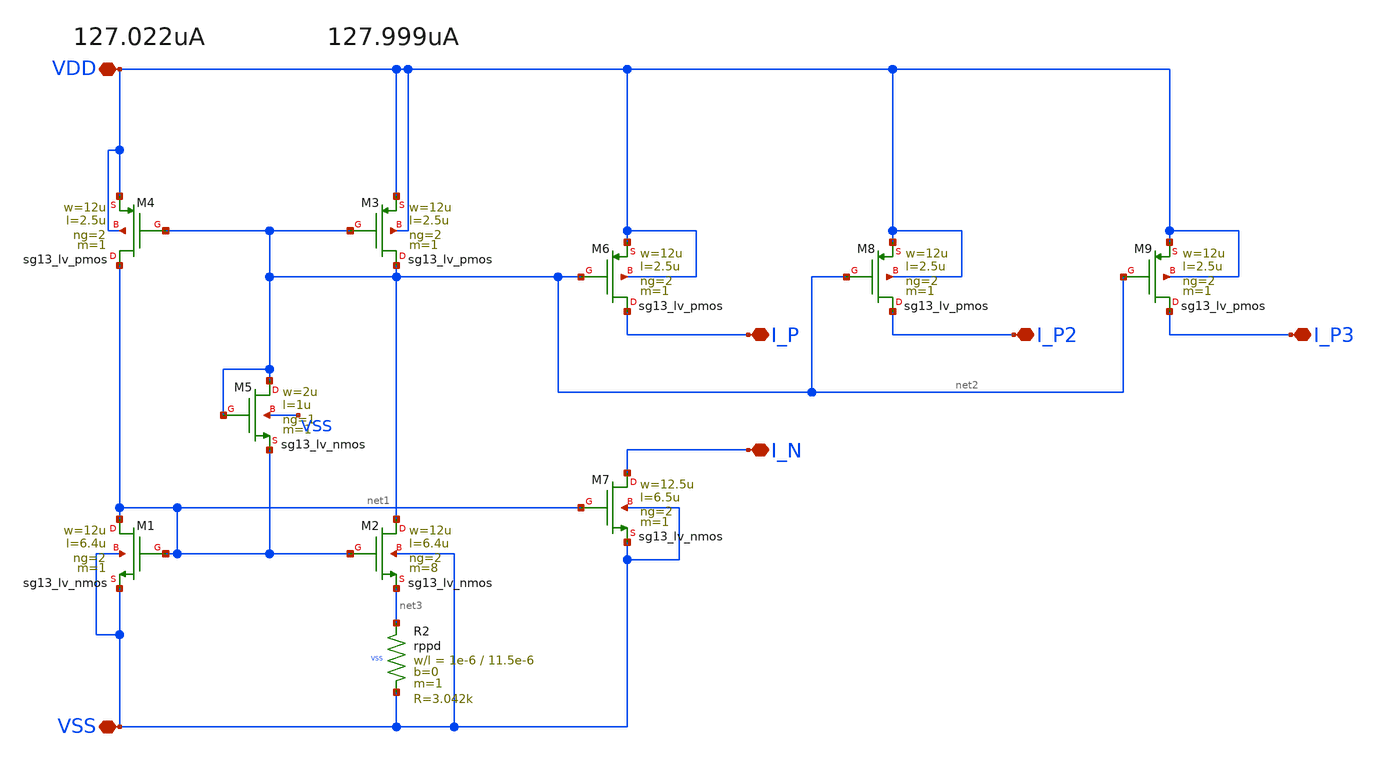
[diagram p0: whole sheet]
** sch_path: OTA_Telescopic_NO_FLATTEN/Schematics_and_Symbols/OTA_Telescopic_currentRef.sch
**.subckt OTA_Telescopic_currentRef VDD VSS I_P I_N I_P2 I_P3
*.iopin VDD
*.iopin VSS
*.iopin I_P
*.iopin I_N
*.iopin I_P2
*.iopin I_P3
XM3 net2 net2 VDD VDD sg13_lv_pmos w=12u l=2.5u ng=2 m=1 mm_ok=1
XM2 net2 net1 net3 VSS sg13_lv_nmos w=12u l=6.4u ng=2 m=8 mm_ok=1
XM4 net1 net2 VDD VDD sg13_lv_pmos w=12u l=2.5u ng=2 m=1 mm_ok=1
XM1 net1 net1 VSS VSS sg13_lv_nmos w=12u l=6.4u ng=2 m=1 mm_ok=1
XM5 net2 net2 net1 VSS sg13_lv_nmos w=2u l=1u ng=1 m=1 mm_ok=1
XR2 net3 VSS VSS rppd w=1e-6 l=11.5e-6 m=1 b=0 mm_ok=1
XM6 I_P net2 VDD VDD sg13_lv_pmos w=12u l=2.5u ng=2 m=1 mm_ok=1
XM7 I_N net1 VSS VSS sg13_lv_nmos w=12.5u l=6.5u ng=2 m=1 mm_ok=1
XM8 I_P2 net2 VDD VDD sg13_lv_pmos w=12u l=2.5u ng=2 m=1 mm_ok=1
XM9 I_P3 net2 VDD VDD sg13_lv_pmos w=12u l=2.5u ng=2 m=1 mm_ok=1
**.ends
.end
